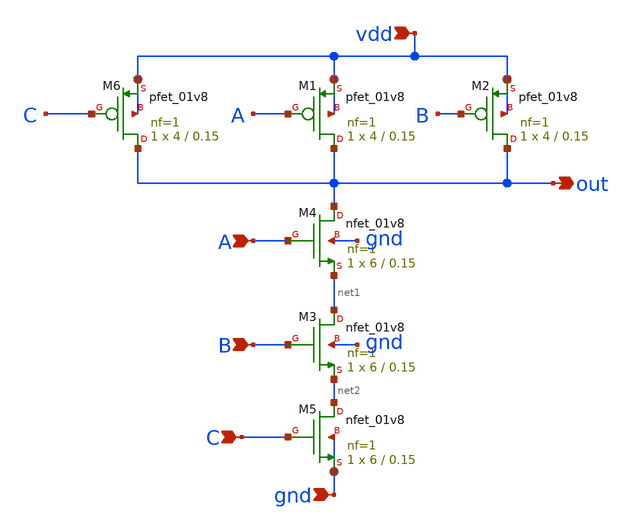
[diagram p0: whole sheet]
** sch_path: pll/Integeration/circuit_integeration/tests/test_div/divider_design/nand_3in/xschem/nand_3in.sch
**.subckt nand_3in vdd A B gnd out C
*.ipin vdd
*.ipin A
*.ipin B
*.ipin gnd
*.opin out
*.ipin C
XM1 out A vdd vdd sky130_fd_pr__pfet_01v8 L=0.15 W=4 nf=1 ad='int((nf+1)/2) * W/nf * 0.29' as='int((nf+2)/2) * W/nf * 0.29'
+ pd='2*int((nf+1)/2) * (W/nf + 0.29)' ps='2*int((nf+2)/2) * (W/nf + 0.29)' nrd='0.29 / W' nrs='0.29 / W'
+ sa=0 sb=0 sd=0 mult=1 m=1
XM2 out B vdd vdd sky130_fd_pr__pfet_01v8 L=0.15 W=4 nf=1 ad='int((nf+1)/2) * W/nf * 0.29' as='int((nf+2)/2) * W/nf * 0.29'
+ pd='2*int((nf+1)/2) * (W/nf + 0.29)' ps='2*int((nf+2)/2) * (W/nf + 0.29)' nrd='0.29 / W' nrs='0.29 / W'
+ sa=0 sb=0 sd=0 mult=1 m=1
XM4 out A net1 gnd sky130_fd_pr__nfet_01v8 L=0.15 W=6 nf=1 ad='int((1 + 1)/2) * 6 / 1 * 0.29' as='int((1 + 2)/2) * 6 / 1 * 0.29'
+ pd='2*int((1 + 1)/2) * (6 / 1 + 0.29)' ps='2*int((1 + 2)/2) * (6 / 1 + 0.29)' nrd='0.29 / 6 ' nrs='0.29 / 6 '
+ sa=0 sb=0 sd=0 mult=1 m=1
XM3 net1 B net2 gnd sky130_fd_pr__nfet_01v8 L=0.15 W=6 nf=1 ad='int((1 + 1)/2) * 6 / 1 * 0.29' as='int((1 + 2)/2) * 6 / 1 * 0.29'
+ pd='2*int((1 + 1)/2) * (6 / 1 + 0.29)' ps='2*int((1 + 2)/2) * (6 / 1 + 0.29)' nrd='0.29 / 6 ' nrs='0.29 / 6 '
+ sa=0 sb=0 sd=0 mult=1 m=1
XM6 out C vdd vdd sky130_fd_pr__pfet_01v8 L=0.15 W=4 nf=1 ad='int((nf+1)/2) * W/nf * 0.29' as='int((nf+2)/2) * W/nf * 0.29'
+ pd='2*int((nf+1)/2) * (W/nf + 0.29)' ps='2*int((nf+2)/2) * (W/nf + 0.29)' nrd='0.29 / W' nrs='0.29 / W'
+ sa=0 sb=0 sd=0 mult=1 m=1
XM5 net2 C gnd gnd sky130_fd_pr__nfet_01v8 L=0.15 W=6 nf=1 ad='int((1 + 1)/2) * 6 / 1 * 0.29' as='int((1 + 2)/2) * 6 / 1 * 0.29'
+ pd='2*int((1 + 1)/2) * (6 / 1 + 0.29)' ps='2*int((1 + 2)/2) * (6 / 1 + 0.29)' nrd='0.29 / 6 ' nrs='0.29 / 6 '
+ sa=0 sb=0 sd=0 mult=1 m=1
**.ends
.end
